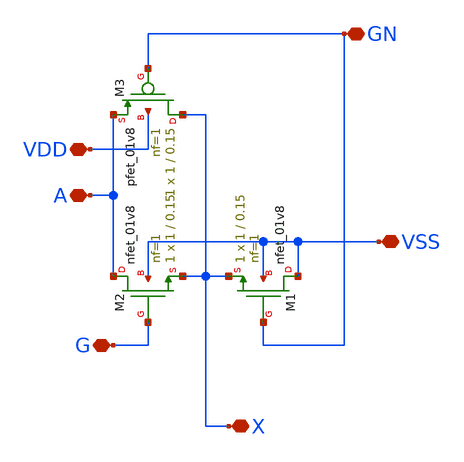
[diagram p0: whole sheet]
** sch_path: GATE.sch
**.subckt GATE GN G A VSS VDD X
*.iopin GN
*.iopin G
*.iopin A
*.iopin VSS
*.iopin VDD
*.iopin X
XM1 VSS GN X VSS sky130_fd_pr__nfet_01v8 L=0.15 W=1 nf=1 ad='int((nf+1)/2) * W/nf * 0.29' as='int((nf+2)/2) * W/nf * 0.29'
+ pd='2*int((nf+1)/2) * (W/nf + 0.29)' ps='2*int((nf+2)/2) * (W/nf + 0.29)' nrd='0.29 / W' nrs='0.29 / W'
+ sa=0 sb=0 sd=0 mult=1 m=1
XM2 A G X VSS sky130_fd_pr__nfet_01v8 L=0.15 W=1 nf=1 ad='int((nf+1)/2) * W/nf * 0.29' as='int((nf+2)/2) * W/nf * 0.29'
+ pd='2*int((nf+1)/2) * (W/nf + 0.29)' ps='2*int((nf+2)/2) * (W/nf + 0.29)' nrd='0.29 / W' nrs='0.29 / W'
+ sa=0 sb=0 sd=0 mult=1 m=1
XM3 X GN A VDD sky130_fd_pr__pfet_01v8 L=0.15 W=1 nf=1 ad='int((nf+1)/2) * W/nf * 0.29' as='int((nf+2)/2) * W/nf * 0.29'
+ pd='2*int((nf+1)/2) * (W/nf + 0.29)' ps='2*int((nf+2)/2) * (W/nf + 0.29)' nrd='0.29 / W' nrs='0.29 / W'
+ sa=0 sb=0 sd=0 mult=1 m=1
**.ends
.end
